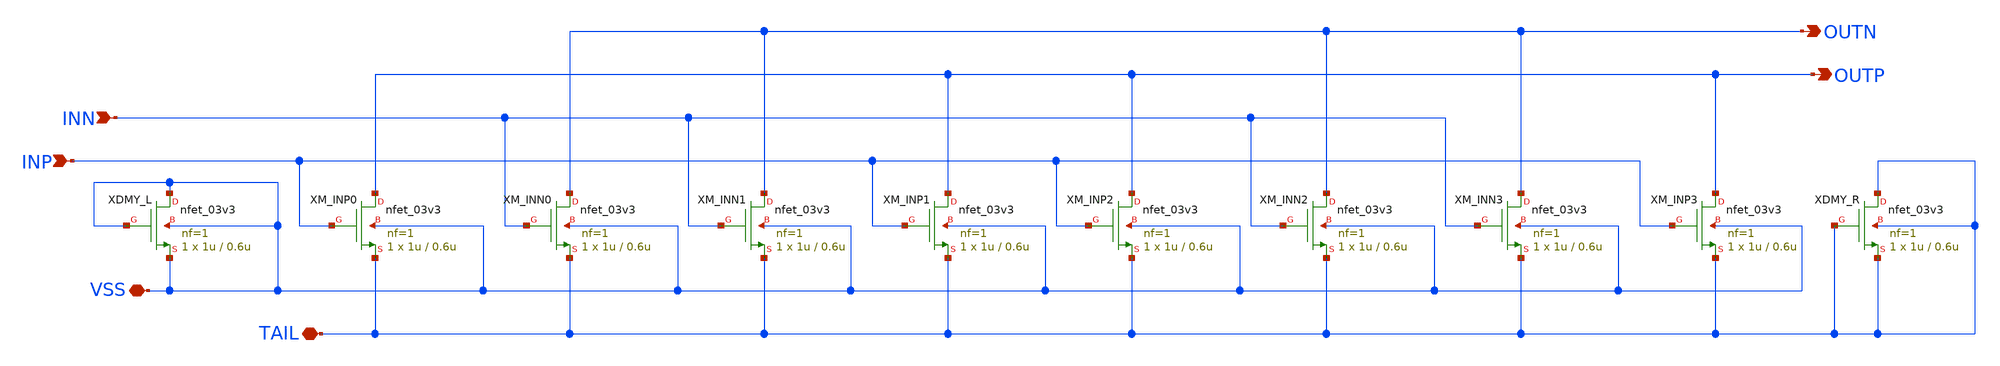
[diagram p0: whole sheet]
** sch_path: designs/libs/core_matchmaker/nmos_diff_pair/matched_nmos_diffpair_4u.sch
**.subckt matched_nmos_diffpair_4u TAIL VSS INN INP OUTN OUTP
*.iopin TAIL
*.iopin VSS
*.ipin INN
*.ipin INP
*.opin OUTN
*.opin OUTP
XM_INP2 OUTP INP TAIL VSS nfet_03v3 L=0.6u W=1u nf=1 ad='int((nf+1)/2) * W/nf * 0.18u' as='int((nf+2)/2) * W/nf * 0.18u'
+ pd='2*int((nf+1)/2) * (W/nf + 0.18u)' ps='2*int((nf+2)/2) * (W/nf + 0.18u)' nrd='0.18u / W' nrs='0.18u / W'
+ sa=0 sb=0 sd=0 m=1
XM_INP1 OUTP INP TAIL VSS nfet_03v3 L=0.6u W=1u nf=1 ad='int((nf+1)/2) * W/nf * 0.18u' as='int((nf+2)/2) * W/nf * 0.18u'
+ pd='2*int((nf+1)/2) * (W/nf + 0.18u)' ps='2*int((nf+2)/2) * (W/nf + 0.18u)' nrd='0.18u / W' nrs='0.18u / W'
+ sa=0 sb=0 sd=0 m=1
XM_INN1 OUTN INN TAIL VSS nfet_03v3 L=0.6u W=1u nf=1 ad='int((nf+1)/2) * W/nf * 0.18u' as='int((nf+2)/2) * W/nf * 0.18u'
+ pd='2*int((nf+1)/2) * (W/nf + 0.18u)' ps='2*int((nf+2)/2) * (W/nf + 0.18u)' nrd='0.18u / W' nrs='0.18u / W'
+ sa=0 sb=0 sd=0 m=1
XM_INN0 OUTN INN TAIL VSS nfet_03v3 L=0.6u W=1u nf=1 ad='int((nf+1)/2) * W/nf * 0.18u' as='int((nf+2)/2) * W/nf * 0.18u'
+ pd='2*int((nf+1)/2) * (W/nf + 0.18u)' ps='2*int((nf+2)/2) * (W/nf + 0.18u)' nrd='0.18u / W' nrs='0.18u / W'
+ sa=0 sb=0 sd=0 m=1
XM_INP0 OUTP INP TAIL VSS nfet_03v3 L=0.6u W=1u nf=1 ad='int((nf+1)/2) * W/nf * 0.18u' as='int((nf+2)/2) * W/nf * 0.18u'
+ pd='2*int((nf+1)/2) * (W/nf + 0.18u)' ps='2*int((nf+2)/2) * (W/nf + 0.18u)' nrd='0.18u / W' nrs='0.18u / W'
+ sa=0 sb=0 sd=0 m=1
XDMY_L VSS VSS VSS VSS nfet_03v3 L=0.6u W=1u nf=1 ad='int((nf+1)/2) * W/nf * 0.18u' as='int((nf+2)/2) * W/nf * 0.18u'
+ pd='2*int((nf+1)/2) * (W/nf + 0.18u)' ps='2*int((nf+2)/2) * (W/nf + 0.18u)' nrd='0.18u / W' nrs='0.18u / W'
+ sa=0 sb=0 sd=0 m=1
XM_INN2 OUTN INN TAIL VSS nfet_03v3 L=0.6u W=1u nf=1 ad='int((nf+1)/2) * W/nf * 0.18u' as='int((nf+2)/2) * W/nf * 0.18u'
+ pd='2*int((nf+1)/2) * (W/nf + 0.18u)' ps='2*int((nf+2)/2) * (W/nf + 0.18u)' nrd='0.18u / W' nrs='0.18u / W'
+ sa=0 sb=0 sd=0 m=1
XM_INN3 OUTN INN TAIL VSS nfet_03v3 L=0.6u W=1u nf=1 ad='int((nf+1)/2) * W/nf * 0.18u' as='int((nf+2)/2) * W/nf * 0.18u'
+ pd='2*int((nf+1)/2) * (W/nf + 0.18u)' ps='2*int((nf+2)/2) * (W/nf + 0.18u)' nrd='0.18u / W' nrs='0.18u / W'
+ sa=0 sb=0 sd=0 m=1
XM_INP3 OUTP INP TAIL VSS nfet_03v3 L=0.6u W=1u nf=1 ad='int((nf+1)/2) * W/nf * 0.18u' as='int((nf+2)/2) * W/nf * 0.18u'
+ pd='2*int((nf+1)/2) * (W/nf + 0.18u)' ps='2*int((nf+2)/2) * (W/nf + 0.18u)' nrd='0.18u / W' nrs='0.18u / W'
+ sa=0 sb=0 sd=0 m=1
XDMY_R TAIL TAIL TAIL TAIL nfet_03v3 L=0.6u W=1u nf=1 ad='int((nf+1)/2) * W/nf * 0.18u' as='int((nf+2)/2) * W/nf * 0.18u'
+ pd='2*int((nf+1)/2) * (W/nf + 0.18u)' ps='2*int((nf+2)/2) * (W/nf + 0.18u)' nrd='0.18u / W' nrs='0.18u / W'
+ sa=0 sb=0 sd=0 m=1
**.ends
.end
